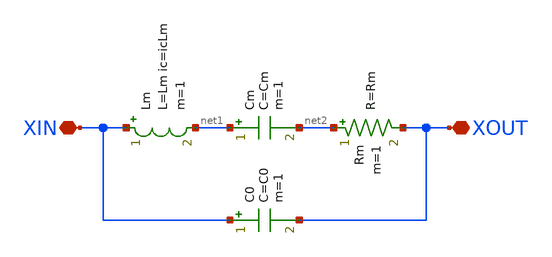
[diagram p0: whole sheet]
** sch_path: xschem/crystal_model.sch
**.subckt crystal_model XIN XOUT
*.iopin XIN
*.iopin XOUT
Cm net1 net2 C=Cm m=1
Lm XIN net1 L=Lm ic=icLm m=1
Rm net2 XOUT R=Rm m=1
C0 XIN XOUT C=C0 m=1
**.ends
.end
